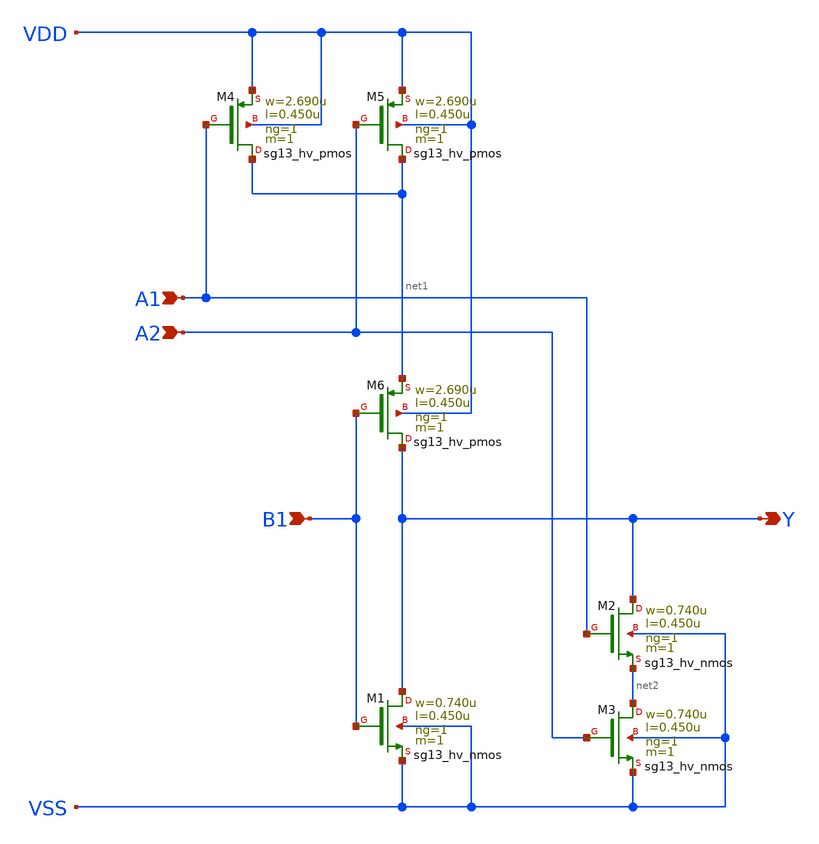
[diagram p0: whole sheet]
** sch_path: ihp-sg13g2/libs.ref/sg13g2_stdcell_hv/sch/xschem/sg13g2_hv_a21oi_1.sch
* Copyright 2023 IHP PDK Authors
* Licensed under the Apache License, Version 2.0 (the "License");
* you may not use this file except in compliance with the License.
* You may obtain a copy of the License at
* https://www.apache.org/licenses/LICENSE-2.0
* Unless required by applicable law or agreed to in writing, software
* distributed under the License is distributed on an "AS IS" BASIS,
* WITHOUT WARRANTIES OR CONDITIONS OF ANY KIND, either express or implied.
* See the License for the specific language governing permissions and
* limitations under the License.
**.subckt sg13g2_hv_a21oi_1 A1 A2 B1 Y
*.ipin A1
*.ipin A2
*.ipin B1
*.opin Y
XM1 Y B1 VSS VSS sg13_hv_nmos w=0.740u l=0.450u ng=1 m=1 mm_ok=1
XM2 Y A1 net2 VSS sg13_hv_nmos w=0.740u l=0.450u ng=1 m=1 mm_ok=1
XM3 net2 A2 VSS VSS sg13_hv_nmos w=0.740u l=0.450u ng=1 m=1 mm_ok=1
XM4 net1 A1 VDD VDD sg13_hv_pmos w=2.690u l=0.450u ng=1 m=1 mm_ok=1
XM5 net1 A2 VDD VDD sg13_hv_pmos w=2.690u l=0.450u ng=1 m=1 mm_ok=1
XM6 Y B1 net1 VDD sg13_hv_pmos w=2.690u l=0.450u ng=1 m=1 mm_ok=1
**.ends
.end
